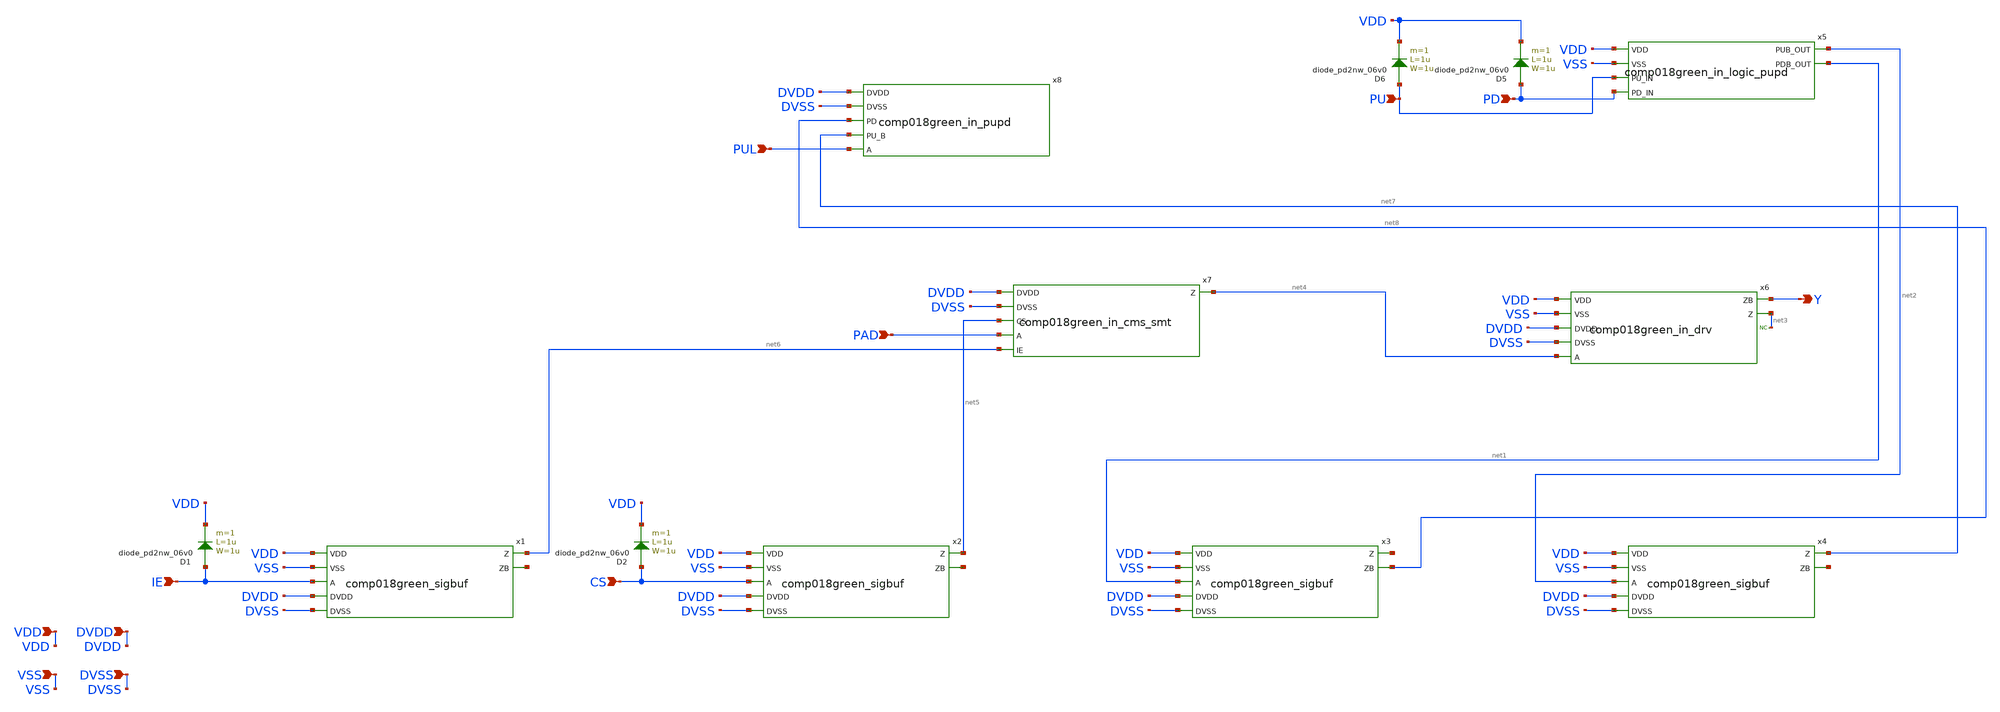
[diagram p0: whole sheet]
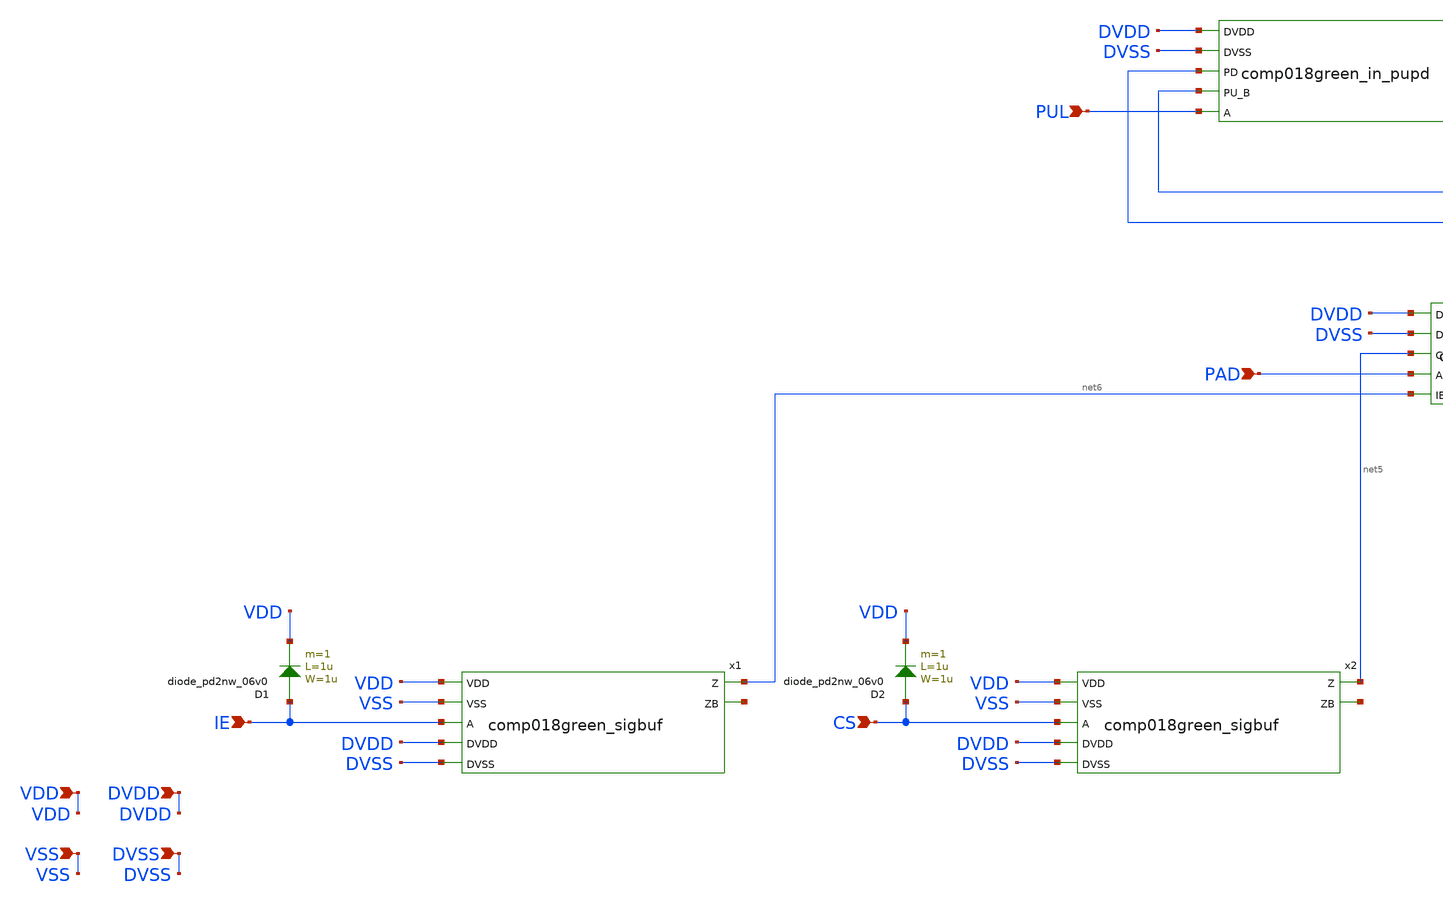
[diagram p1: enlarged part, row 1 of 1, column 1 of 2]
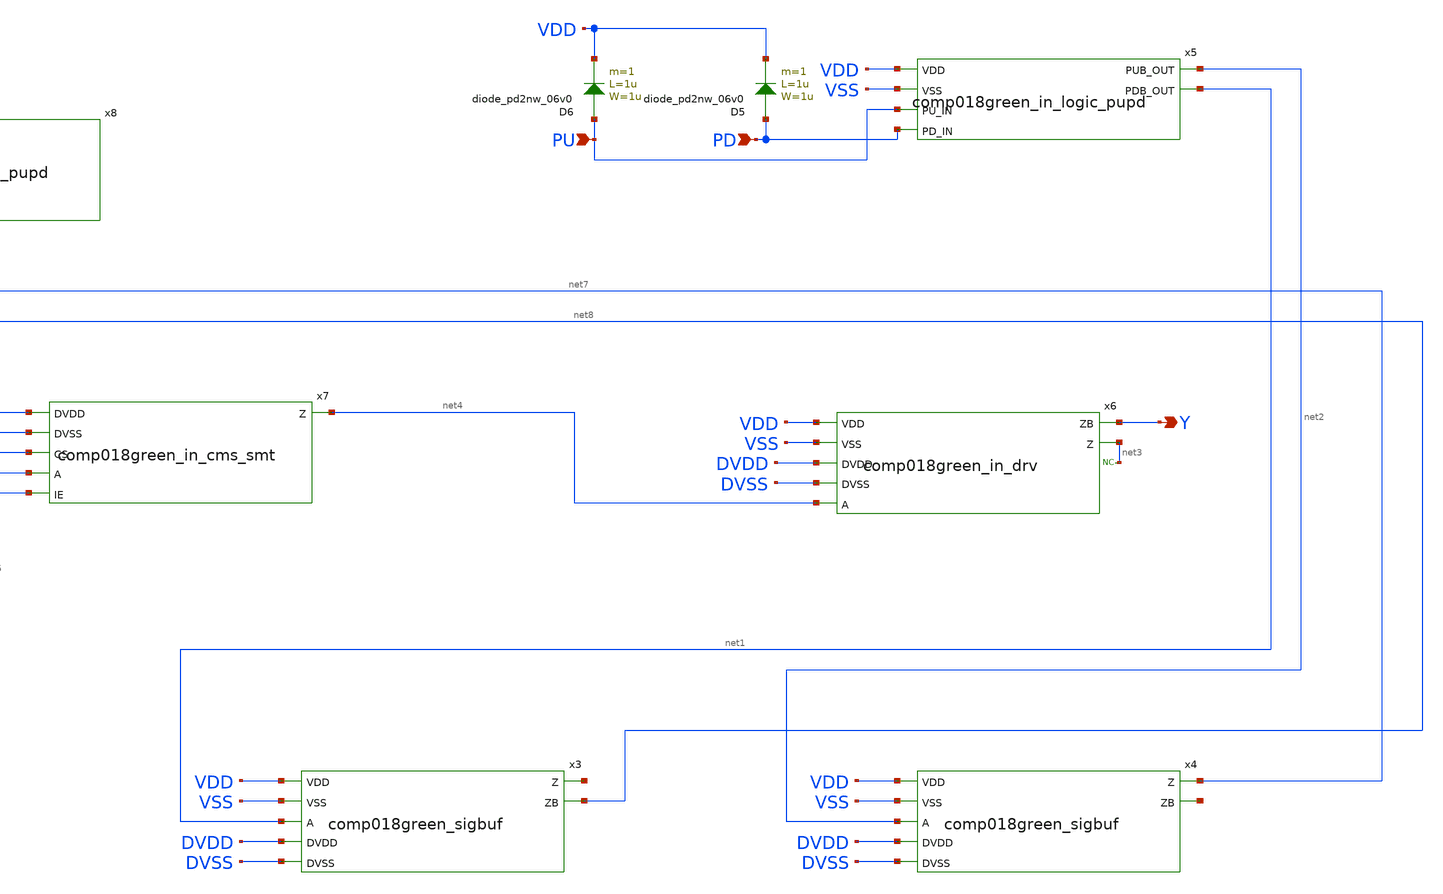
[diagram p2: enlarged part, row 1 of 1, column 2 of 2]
** sch_path: gf180mcu_fd_io__bi_24t/comp018green_inpath_cms_smt.sch
**.subckt comp018green_inpath_cms_smt IE CS VDD VSS DVDD DVSS PU PD Y PAD PUL
*.ipin IE
*.ipin CS
*.ipin VDD
*.ipin VSS
*.ipin DVDD
*.ipin DVSS
*.ipin PU
*.ipin PD
*.opin Y
*.ipin PAD
*.ipin PUL
x1 DVDD VDD net6 IE net9 DVSS VSS comp018green_sigbuf
x2 DVDD VDD net5 CS net10 DVSS VSS comp018green_sigbuf
x3 DVDD VDD net11 net1 net8 DVSS VSS comp018green_sigbuf
x4 DVDD VDD net7 net2 net12 DVSS VSS comp018green_sigbuf
D1 IE VDD diode_pd2nw_06v0 area='1u * 1u ' pj='2*1u + 2*1u ' m=1
D2 CS VDD diode_pd2nw_06v0 area='1u * 1u ' pj='2*1u + 2*1u ' m=1
x5 net2 net1 PU VDD PD VSS comp018green_in_logic_pupd
D5 PD VDD diode_pd2nw_06v0 area='1u * 1u ' pj='2*1u + 2*1u ' m=1
D6 PU VDD diode_pd2nw_06v0 area='1u * 1u ' pj='2*1u + 2*1u ' m=1
x6 Y VDD net3 net4 DVDD DVSS VSS comp018green_in_drv
* noconn #net3
x7 DVDD net4 DVSS net5 PAD net6 comp018green_in_cms_smt
x8 DVSS DVDD net8 net7 PUL comp018green_in_pupd
**.ends

* expanding   symbol:  comp018green_sigbuf.sym # of pins=7
** sym_path: gf180mcu_fd_io__bi_24t/comp018green_sigbuf.sym
** sch_path: gf180mcu_fd_io__bi_24t/comp018green_sigbuf.sch
.subckt comp018green_sigbuf DVDD VDD Z A ZB DVSS VSS
*.ipin VDD
*.ipin VSS
*.ipin A
*.ipin DVSS
*.ipin DVDD
*.opin Z
*.opin ZB
XM1 net1 A VSS VSS nfet_06v0 L=0.70u W=1.5u nf=1 ad='int((nf+1)/2) * W/nf * 0.18u' as='int((nf+2)/2) * W/nf * 0.18u'
+ pd='2*int((nf+1)/2) * (W/nf + 0.18u)' ps='2*int((nf+2)/2) * (W/nf + 0.18u)' nrd='0.18u / W' nrs='0.18u / W'
+ sa=0 sb=0 sd=0 m=1
XM2 net1 A VDD VDD pfet_06v0 L=0.70u W=3u nf=1 ad='int((nf+1)/2) * W/nf * 0.18u' as='int((nf+2)/2) * W/nf * 0.18u'
+ pd='2*int((nf+1)/2) * (W/nf + 0.18u)' ps='2*int((nf+2)/2) * (W/nf + 0.18u)' nrd='0.18u / W' nrs='0.18u / W'
+ sa=0 sb=0 sd=0 m=1
XM3 Z net1 DVDD DVDD pfet_06v0 L=0.70u W=3u nf=1 ad='int((nf+1)/2) * W/nf * 0.18u' as='int((nf+2)/2) * W/nf * 0.18u'
+ pd='2*int((nf+1)/2) * (W/nf + 0.18u)' ps='2*int((nf+2)/2) * (W/nf + 0.18u)' nrd='0.18u / W' nrs='0.18u / W'
+ sa=0 sb=0 sd=0 m=1
XM4 Z net1 DVSS DVSS nfet_06v0 L=0.70u W=1.5u nf=1 ad='int((nf+1)/2) * W/nf * 0.18u' as='int((nf+2)/2) * W/nf * 0.18u'
+ pd='2*int((nf+1)/2) * (W/nf + 0.18u)' ps='2*int((nf+2)/2) * (W/nf + 0.18u)' nrd='0.18u / W' nrs='0.18u / W'
+ sa=0 sb=0 sd=0 m=1
XM5 Z net1 DVDD DVDD pfet_06v0 L=0.70u W=3u nf=1 ad='int((nf+1)/2) * W/nf * 0.18u' as='int((nf+2)/2) * W/nf * 0.18u'
+ pd='2*int((nf+1)/2) * (W/nf + 0.18u)' ps='2*int((nf+2)/2) * (W/nf + 0.18u)' nrd='0.18u / W' nrs='0.18u / W'
+ sa=0 sb=0 sd=0 m=1
XM6 ZB Z DVDD DVDD pfet_06v0 L=0.70u W=3u nf=1 ad='int((nf+1)/2) * W/nf * 0.18u' as='int((nf+2)/2) * W/nf * 0.18u'
+ pd='2*int((nf+1)/2) * (W/nf + 0.18u)' ps='2*int((nf+2)/2) * (W/nf + 0.18u)' nrd='0.18u / W' nrs='0.18u / W'
+ sa=0 sb=0 sd=0 m=1
XM7 ZB Z DVDD DVDD pfet_06v0 L=0.70u W=3u nf=1 ad='int((nf+1)/2) * W/nf * 0.18u' as='int((nf+2)/2) * W/nf * 0.18u'
+ pd='2*int((nf+1)/2) * (W/nf + 0.18u)' ps='2*int((nf+2)/2) * (W/nf + 0.18u)' nrd='0.18u / W' nrs='0.18u / W'
+ sa=0 sb=0 sd=0 m=1
XM8 Z net1 DVSS DVSS nfet_06v0 L=0.70u W=1.5u nf=1 ad='int((nf+1)/2) * W/nf * 0.18u' as='int((nf+2)/2) * W/nf * 0.18u'
+ pd='2*int((nf+1)/2) * (W/nf + 0.18u)' ps='2*int((nf+2)/2) * (W/nf + 0.18u)' nrd='0.18u / W' nrs='0.18u / W'
+ sa=0 sb=0 sd=0 m=1
XM9 ZB Z DVSS DVSS nfet_06v0 L=0.70u W=1.5u nf=1 ad='int((nf+1)/2) * W/nf * 0.18u' as='int((nf+2)/2) * W/nf * 0.18u'
+ pd='2*int((nf+1)/2) * (W/nf + 0.18u)' ps='2*int((nf+2)/2) * (W/nf + 0.18u)' nrd='0.18u / W' nrs='0.18u / W'
+ sa=0 sb=0 sd=0 m=1
XM10 ZB Z DVSS DVSS nfet_06v0 L=0.70u W=1.5u nf=1 ad='int((nf+1)/2) * W/nf * 0.18u' as='int((nf+2)/2) * W/nf * 0.18u'
+ pd='2*int((nf+1)/2) * (W/nf + 0.18u)' ps='2*int((nf+2)/2) * (W/nf + 0.18u)' nrd='0.18u / W' nrs='0.18u / W'
+ sa=0 sb=0 sd=0 m=1
.ends


* expanding   symbol:  comp018green_in_logic_pupd.sym # of pins=6
** sym_path: gf180mcu_fd_io__bi_24t/comp018green_in_logic_pupd.sym
** sch_path: gf180mcu_fd_io__bi_24t/comp018green_in_logic_pupd.sch
.subckt comp018green_in_logic_pupd PUB_OUT PDB_OUT PU_IN VDD PD_IN VSS
*.ipin VDD
*.ipin VSS
*.ipin PD_IN
*.ipin PU_IN
*.opin PUB_OUT
*.opin PDB_OUT
XM1 net1 PU_IN VSS net6 nfet_06v0 L=0.70u W=1.5u nf=1 ad='int((nf+1)/2) * W/nf * 0.18u' as='int((nf+2)/2) * W/nf * 0.18u'
+ pd='2*int((nf+1)/2) * (W/nf + 0.18u)' ps='2*int((nf+2)/2) * (W/nf + 0.18u)' nrd='0.18u / W' nrs='0.18u / W'
+ sa=0 sb=0 sd=0 m=1
XM2 PU_IN net3 net2 net7 nfet_06v0 L=0.70u W=1.5u nf=1 ad='int((nf+1)/2) * W/nf * 0.18u' as='int((nf+2)/2) * W/nf * 0.18u'
+ pd='2*int((nf+1)/2) * (W/nf + 0.18u)' ps='2*int((nf+2)/2) * (W/nf + 0.18u)' nrd='0.18u / W' nrs='0.18u / W'
+ sa=0 sb=0 sd=0 m=1
XM3 net1 PD_IN net2 net8 nfet_06v0 L=0.70u W=1.5u nf=1 ad='int((nf+1)/2) * W/nf * 0.18u' as='int((nf+2)/2) * W/nf * 0.18u'
+ pd='2*int((nf+1)/2) * (W/nf + 0.18u)' ps='2*int((nf+2)/2) * (W/nf + 0.18u)' nrd='0.18u / W' nrs='0.18u / W'
+ sa=0 sb=0 sd=0 m=1
XM4 net3 PD_IN VSS net9 nfet_06v0 L=0.70u W=1.5u nf=1 ad='int((nf+1)/2) * W/nf * 0.18u' as='int((nf+2)/2) * W/nf * 0.18u'
+ pd='2*int((nf+1)/2) * (W/nf + 0.18u)' ps='2*int((nf+2)/2) * (W/nf + 0.18u)' nrd='0.18u / W' nrs='0.18u / W'
+ sa=0 sb=0 sd=0 m=1
XM5 net1 PU_IN VDD net10 pfet_06v0 L=0.70u W=3u nf=1 ad='int((nf+1)/2) * W/nf * 0.18u' as='int((nf+2)/2) * W/nf * 0.18u'
+ pd='2*int((nf+1)/2) * (W/nf + 0.18u)' ps='2*int((nf+2)/2) * (W/nf + 0.18u)' nrd='0.18u / W' nrs='0.18u / W'
+ sa=0 sb=0 sd=0 m=1
XM6 PU_IN PD_IN net2 net11 pfet_06v0 L=0.70u W=3u nf=1 ad='int((nf+1)/2) * W/nf * 0.18u' as='int((nf+2)/2) * W/nf * 0.18u'
+ pd='2*int((nf+1)/2) * (W/nf + 0.18u)' ps='2*int((nf+2)/2) * (W/nf + 0.18u)' nrd='0.18u / W' nrs='0.18u / W'
+ sa=0 sb=0 sd=0 m=1
XM7 net12 net3 net2 net13 pfet_06v0 L=0.70u W=3u nf=1 ad='int((nf+1)/2) * W/nf * 0.18u' as='int((nf+2)/2) * W/nf * 0.18u'
+ pd='2*int((nf+1)/2) * (W/nf + 0.18u)' ps='2*int((nf+2)/2) * (W/nf + 0.18u)' nrd='0.18u / W' nrs='0.18u / W'
+ sa=0 sb=0 sd=0 m=1
XM8 net3 PD_IN VDD net14 pfet_06v0 L=0.70u W=3u nf=1 ad='int((nf+1)/2) * W/nf * 0.18u' as='int((nf+2)/2) * W/nf * 0.18u'
+ pd='2*int((nf+1)/2) * (W/nf + 0.18u)' ps='2*int((nf+2)/2) * (W/nf + 0.18u)' nrd='0.18u / W' nrs='0.18u / W'
+ sa=0 sb=0 sd=0 m=1
XM9 PUB_OUT PU_IN VDD net15 pfet_06v0 L=0.70u W=3u nf=1 ad='int((nf+1)/2) * W/nf * 0.18u' as='int((nf+2)/2) * W/nf * 0.18u'
+ pd='2*int((nf+1)/2) * (W/nf + 0.18u)' ps='2*int((nf+2)/2) * (W/nf + 0.18u)' nrd='0.18u / W' nrs='0.18u / W'
+ sa=0 sb=0 sd=0 m=1
XM10 PUB_OUT net2 VDD net16 pfet_06v0 L=0.70u W=3u nf=1 ad='int((nf+1)/2) * W/nf * 0.18u' as='int((nf+2)/2) * W/nf * 0.18u'
+ pd='2*int((nf+1)/2) * (W/nf + 0.18u)' ps='2*int((nf+2)/2) * (W/nf + 0.18u)' nrd='0.18u / W' nrs='0.18u / W'
+ sa=0 sb=0 sd=0 m=1
XM11 PDB_OUT net2 VDD net17 pfet_06v0 L=0.70u W=3u nf=1 ad='int((nf+1)/2) * W/nf * 0.18u' as='int((nf+2)/2) * W/nf * 0.18u'
+ pd='2*int((nf+1)/2) * (W/nf + 0.18u)' ps='2*int((nf+2)/2) * (W/nf + 0.18u)' nrd='0.18u / W' nrs='0.18u / W'
+ sa=0 sb=0 sd=0 m=1
XM12 PDB_OUT PD_IN VDD net18 pfet_06v0 L=0.70u W=3u nf=1 ad='int((nf+1)/2) * W/nf * 0.18u' as='int((nf+2)/2) * W/nf * 0.18u'
+ pd='2*int((nf+1)/2) * (W/nf + 0.18u)' ps='2*int((nf+2)/2) * (W/nf + 0.18u)' nrd='0.18u / W' nrs='0.18u / W'
+ sa=0 sb=0 sd=0 m=1
XM13 net4 PU_IN VSS net19 nfet_06v0 L=0.70u W=3u nf=1 ad='int((nf+1)/2) * W/nf * 0.18u' as='int((nf+2)/2) * W/nf * 0.18u'
+ pd='2*int((nf+1)/2) * (W/nf + 0.18u)' ps='2*int((nf+2)/2) * (W/nf + 0.18u)' nrd='0.18u / W' nrs='0.18u / W'
+ sa=0 sb=0 sd=0 m=1
XM14 net4 net2 PUB_OUT net20 nfet_06v0 L=0.70u W=3u nf=1 ad='int((nf+1)/2) * W/nf * 0.18u' as='int((nf+2)/2) * W/nf * 0.18u'
+ pd='2*int((nf+1)/2) * (W/nf + 0.18u)' ps='2*int((nf+2)/2) * (W/nf + 0.18u)' nrd='0.18u / W' nrs='0.18u / W'
+ sa=0 sb=0 sd=0 m=1
XM15 net5 net2 VSS net21 nfet_06v0 L=0.70u W=3u nf=1 ad='int((nf+1)/2) * W/nf * 0.18u' as='int((nf+2)/2) * W/nf * 0.18u'
+ pd='2*int((nf+1)/2) * (W/nf + 0.18u)' ps='2*int((nf+2)/2) * (W/nf + 0.18u)' nrd='0.18u / W' nrs='0.18u / W'
+ sa=0 sb=0 sd=0 m=1
XM16 net5 PD_IN PDB_OUT net22 nfet_06v0 L=0.70u W=3u nf=1 ad='int((nf+1)/2) * W/nf * 0.18u' as='int((nf+2)/2) * W/nf * 0.18u'
+ pd='2*int((nf+1)/2) * (W/nf + 0.18u)' ps='2*int((nf+2)/2) * (W/nf + 0.18u)' nrd='0.18u / W' nrs='0.18u / W'
+ sa=0 sb=0 sd=0 m=1
.ends


* expanding   symbol:  comp018green_in_drv.sym # of pins=7
** sym_path: gf180mcu_fd_io__bi_24t/comp018green_in_drv.sym
** sch_path: gf180mcu_fd_io__bi_24t/comp018green_in_drv.sch
.subckt comp018green_in_drv ZB VDD Z A DVDD DVSS VSS
*.ipin A
*.ipin DVDD
*.ipin DVSS
*.opin Z
*.opin ZB
*.ipin VDD
*.ipin VSS
XM1 DVSS A net1 net2 nfet_06v0 L=0.70u W=4u nf=1 ad='int((nf+1)/2) * W/nf * 0.18u' as='int((nf+2)/2) * W/nf * 0.18u'
+ pd='2*int((nf+1)/2) * (W/nf + 0.18u)' ps='2*int((nf+2)/2) * (W/nf + 0.18u)' nrd='0.18u / W' nrs='0.18u / W'
+ sa=0 sb=0 sd=0 m=1
XM3 net1 A DVDD net3 pfet_06v0 L=0.70u W=2u nf=1 ad='int((nf+1)/2) * W/nf * 0.18u' as='int((nf+2)/2) * W/nf * 0.18u'
+ pd='2*int((nf+1)/2) * (W/nf + 0.18u)' ps='2*int((nf+2)/2) * (W/nf + 0.18u)' nrd='0.18u / W' nrs='0.18u / W'
+ sa=0 sb=0 sd=0 m=1
XM2 DVSS A net1 net4 nfet_06v0 L=0.70u W=4u nf=1 ad='int((nf+1)/2) * W/nf * 0.18u' as='int((nf+2)/2) * W/nf * 0.18u'
+ pd='2*int((nf+1)/2) * (W/nf + 0.18u)' ps='2*int((nf+2)/2) * (W/nf + 0.18u)' nrd='0.18u / W' nrs='0.18u / W'
+ sa=0 sb=0 sd=0 m=1
XM4 Z net1 VDD net5 pfet_06v0 L=0.70u W=2.5u nf=1 ad='int((nf+1)/2) * W/nf * 0.18u' as='int((nf+2)/2) * W/nf * 0.18u'
+ pd='2*int((nf+1)/2) * (W/nf + 0.18u)' ps='2*int((nf+2)/2) * (W/nf + 0.18u)' nrd='0.18u / W' nrs='0.18u / W'
+ sa=0 sb=0 sd=0 m=1
XM5 Z net1 VDD net6 pfet_06v0 L=0.70u W=2.5u nf=1 ad='int((nf+1)/2) * W/nf * 0.18u' as='int((nf+2)/2) * W/nf * 0.18u'
+ pd='2*int((nf+1)/2) * (W/nf + 0.18u)' ps='2*int((nf+2)/2) * (W/nf + 0.18u)' nrd='0.18u / W' nrs='0.18u / W'
+ sa=0 sb=0 sd=0 m=1
XM6 Z net1 VDD net7 pfet_06v0 L=0.70u W=2.5u nf=1 ad='int((nf+1)/2) * W/nf * 0.18u' as='int((nf+2)/2) * W/nf * 0.18u'
+ pd='2*int((nf+1)/2) * (W/nf + 0.18u)' ps='2*int((nf+2)/2) * (W/nf + 0.18u)' nrd='0.18u / W' nrs='0.18u / W'
+ sa=0 sb=0 sd=0 m=1
XM7 Z net1 VDD net8 pfet_06v0 L=0.70u W=2.5u nf=1 ad='int((nf+1)/2) * W/nf * 0.18u' as='int((nf+2)/2) * W/nf * 0.18u'
+ pd='2*int((nf+1)/2) * (W/nf + 0.18u)' ps='2*int((nf+2)/2) * (W/nf + 0.18u)' nrd='0.18u / W' nrs='0.18u / W'
+ sa=0 sb=0 sd=0 m=1
XM8 Z net1 VSS net9 nfet_06v0 L=0.70u W=1.25u nf=1 ad='int((nf+1)/2) * W/nf * 0.18u' as='int((nf+2)/2) * W/nf * 0.18u'
+ pd='2*int((nf+1)/2) * (W/nf + 0.18u)' ps='2*int((nf+2)/2) * (W/nf + 0.18u)' nrd='0.18u / W' nrs='0.18u / W'
+ sa=0 sb=0 sd=0 m=1
XM9 Z net1 VSS net10 nfet_06v0 L=0.70u W=1.25u nf=1 ad='int((nf+1)/2) * W/nf * 0.18u' as='int((nf+2)/2) * W/nf * 0.18u'
+ pd='2*int((nf+1)/2) * (W/nf + 0.18u)' ps='2*int((nf+2)/2) * (W/nf + 0.18u)' nrd='0.18u / W' nrs='0.18u / W'
+ sa=0 sb=0 sd=0 m=1
XM10 ZB Z VDD net11 pfet_06v0 L=0.70u W=3.5u nf=1 ad='int((nf+1)/2) * W/nf * 0.18u' as='int((nf+2)/2) * W/nf * 0.18u'
+ pd='2*int((nf+1)/2) * (W/nf + 0.18u)' ps='2*int((nf+2)/2) * (W/nf + 0.18u)' nrd='0.18u / W' nrs='0.18u / W'
+ sa=0 sb=0 sd=0 m=1
XM11 ZB Z VSS net12 nfet_06v0 L=0.70u W=1.5u nf=1 ad='int((nf+1)/2) * W/nf * 0.18u' as='int((nf+2)/2) * W/nf * 0.18u'
+ pd='2*int((nf+1)/2) * (W/nf + 0.18u)' ps='2*int((nf+2)/2) * (W/nf + 0.18u)' nrd='0.18u / W' nrs='0.18u / W'
+ sa=0 sb=0 sd=0 m=1
XM12 ZB Z VDD net13 pfet_06v0 L=0.70u W=3.5u nf=1 ad='int((nf+1)/2) * W/nf * 0.18u' as='int((nf+2)/2) * W/nf * 0.18u'
+ pd='2*int((nf+1)/2) * (W/nf + 0.18u)' ps='2*int((nf+2)/2) * (W/nf + 0.18u)' nrd='0.18u / W' nrs='0.18u / W'
+ sa=0 sb=0 sd=0 m=1
XM13 ZB Z VDD net14 pfet_06v0 L=0.70u W=3.5u nf=1 ad='int((nf+1)/2) * W/nf * 0.18u' as='int((nf+2)/2) * W/nf * 0.18u'
+ pd='2*int((nf+1)/2) * (W/nf + 0.18u)' ps='2*int((nf+2)/2) * (W/nf + 0.18u)' nrd='0.18u / W' nrs='0.18u / W'
+ sa=0 sb=0 sd=0 m=1
XM14 ZB Z VDD net15 pfet_06v0 L=0.70u W=3.5u nf=1 ad='int((nf+1)/2) * W/nf * 0.18u' as='int((nf+2)/2) * W/nf * 0.18u'
+ pd='2*int((nf+1)/2) * (W/nf + 0.18u)' ps='2*int((nf+2)/2) * (W/nf + 0.18u)' nrd='0.18u / W' nrs='0.18u / W'
+ sa=0 sb=0 sd=0 m=1
XM15 ZB Z VDD net16 pfet_06v0 L=0.70u W=3.5u nf=1 ad='int((nf+1)/2) * W/nf * 0.18u' as='int((nf+2)/2) * W/nf * 0.18u'
+ pd='2*int((nf+1)/2) * (W/nf + 0.18u)' ps='2*int((nf+2)/2) * (W/nf + 0.18u)' nrd='0.18u / W' nrs='0.18u / W'
+ sa=0 sb=0 sd=0 m=1
XM16 ZB Z VDD net17 pfet_06v0 L=0.70u W=3.5u nf=1 ad='int((nf+1)/2) * W/nf * 0.18u' as='int((nf+2)/2) * W/nf * 0.18u'
+ pd='2*int((nf+1)/2) * (W/nf + 0.18u)' ps='2*int((nf+2)/2) * (W/nf + 0.18u)' nrd='0.18u / W' nrs='0.18u / W'
+ sa=0 sb=0 sd=0 m=1
XM17 ZB Z VSS net18 nfet_06v0 L=0.70u W=1.5u nf=1 ad='int((nf+1)/2) * W/nf * 0.18u' as='int((nf+2)/2) * W/nf * 0.18u'
+ pd='2*int((nf+1)/2) * (W/nf + 0.18u)' ps='2*int((nf+2)/2) * (W/nf + 0.18u)' nrd='0.18u / W' nrs='0.18u / W'
+ sa=0 sb=0 sd=0 m=1
XM18 ZB Z VSS net19 nfet_06v0 L=0.70u W=1.5u nf=1 ad='int((nf+1)/2) * W/nf * 0.18u' as='int((nf+2)/2) * W/nf * 0.18u'
+ pd='2*int((nf+1)/2) * (W/nf + 0.18u)' ps='2*int((nf+2)/2) * (W/nf + 0.18u)' nrd='0.18u / W' nrs='0.18u / W'
+ sa=0 sb=0 sd=0 m=1
XM19 ZB Z VSS net20 nfet_06v0 L=0.70u W=1.5u nf=1 ad='int((nf+1)/2) * W/nf * 0.18u' as='int((nf+2)/2) * W/nf * 0.18u'
+ pd='2*int((nf+1)/2) * (W/nf + 0.18u)' ps='2*int((nf+2)/2) * (W/nf + 0.18u)' nrd='0.18u / W' nrs='0.18u / W'
+ sa=0 sb=0 sd=0 m=1
XM20 ZB Z VSS net21 nfet_06v0 L=0.70u W=1.5u nf=1 ad='int((nf+1)/2) * W/nf * 0.18u' as='int((nf+2)/2) * W/nf * 0.18u'
+ pd='2*int((nf+1)/2) * (W/nf + 0.18u)' ps='2*int((nf+2)/2) * (W/nf + 0.18u)' nrd='0.18u / W' nrs='0.18u / W'
+ sa=0 sb=0 sd=0 m=1
XM21 ZB Z VSS net22 nfet_06v0 L=0.70u W=1.5u nf=1 ad='int((nf+1)/2) * W/nf * 0.18u' as='int((nf+2)/2) * W/nf * 0.18u'
+ pd='2*int((nf+1)/2) * (W/nf + 0.18u)' ps='2*int((nf+2)/2) * (W/nf + 0.18u)' nrd='0.18u / W' nrs='0.18u / W'
+ sa=0 sb=0 sd=0 m=1
.ends


* expanding   symbol:  comp018green_in_cms_smt.sym # of pins=6
** sym_path: gf180mcu_fd_io__bi_24t/comp018green_in_cms_smt.sym
** sch_path: gf180mcu_fd_io__bi_24t/comp018green_in_cms_smt.sch
.subckt comp018green_in_cms_smt DVDD Z DVSS CS A IE
*.ipin CS
*.ipin IE
*.opin Z
*.ipin A
*.ipin DVDD
*.ipin DVSS
XM1 net1 CS DVSS net7 nfet_06v0 L=0.70u W=2u nf=1 ad='int((nf+1)/2) * W/nf * 0.18u' as='int((nf+2)/2) * W/nf * 0.18u'
+ pd='2*int((nf+1)/2) * (W/nf + 0.18u)' ps='2*int((nf+2)/2) * (W/nf + 0.18u)' nrd='0.18u / W' nrs='0.18u / W'
+ sa=0 sb=0 sd=0 m=1
XM2 net1 CS DVSS net8 nfet_06v0 L=0.70u W=2u nf=1 ad='int((nf+1)/2) * W/nf * 0.18u' as='int((nf+2)/2) * W/nf * 0.18u'
+ pd='2*int((nf+1)/2) * (W/nf + 0.18u)' ps='2*int((nf+2)/2) * (W/nf + 0.18u)' nrd='0.18u / W' nrs='0.18u / W'
+ sa=0 sb=0 sd=0 m=1
XM3 net1 CS DVDD net9 pfet_06v0 L=0.70u W=4u nf=1 ad='int((nf+1)/2) * W/nf * 0.18u' as='int((nf+2)/2) * W/nf * 0.18u'
+ pd='2*int((nf+1)/2) * (W/nf + 0.18u)' ps='2*int((nf+2)/2) * (W/nf + 0.18u)' nrd='0.18u / W' nrs='0.18u / W'
+ sa=0 sb=0 sd=0 m=1
XM4 net1 CS DVDD net10 pfet_06v0 L=0.70u W=4u nf=1 ad='int((nf+1)/2) * W/nf * 0.18u' as='int((nf+2)/2) * W/nf * 0.18u'
+ pd='2*int((nf+1)/2) * (W/nf + 0.18u)' ps='2*int((nf+2)/2) * (W/nf + 0.18u)' nrd='0.18u / W' nrs='0.18u / W'
+ sa=0 sb=0 sd=0 m=1
XM5 net6 net1 DVSS net11 nfet_06v0 L=0.70u W=1.5u nf=1 ad='int((nf+1)/2) * W/nf * 0.18u' as='int((nf+2)/2) * W/nf * 0.18u'
+ pd='2*int((nf+1)/2) * (W/nf + 0.18u)' ps='2*int((nf+2)/2) * (W/nf + 0.18u)' nrd='0.18u / W' nrs='0.18u / W'
+ sa=0 sb=0 sd=0 m=1
XM6 net2 IE DVSS net12 nfet_06v0 L=0.70u W=3.2u nf=1 ad='int((nf+1)/2) * W/nf * 0.18u' as='int((nf+2)/2) * W/nf * 0.18u'
+ pd='2*int((nf+1)/2) * (W/nf + 0.18u)' ps='2*int((nf+2)/2) * (W/nf + 0.18u)' nrd='0.18u / W' nrs='0.18u / W'
+ sa=0 sb=0 sd=0 m=1
XM7 net2 IE DVSS net13 nfet_06v0 L=0.70u W=3.2u nf=1 ad='int((nf+1)/2) * W/nf * 0.18u' as='int((nf+2)/2) * W/nf * 0.18u'
+ pd='2*int((nf+1)/2) * (W/nf + 0.18u)' ps='2*int((nf+2)/2) * (W/nf + 0.18u)' nrd='0.18u / W' nrs='0.18u / W'
+ sa=0 sb=0 sd=0 m=1
XM8 net2 IE DVSS net14 nfet_06v0 L=0.70u W=3.2u nf=1 ad='int((nf+1)/2) * W/nf * 0.18u' as='int((nf+2)/2) * W/nf * 0.18u'
+ pd='2*int((nf+1)/2) * (W/nf + 0.18u)' ps='2*int((nf+2)/2) * (W/nf + 0.18u)' nrd='0.18u / W' nrs='0.18u / W'
+ sa=0 sb=0 sd=0 m=1
XM9 net2 IE DVSS net15 nfet_06v0 L=0.70u W=3.2u nf=1 ad='int((nf+1)/2) * W/nf * 0.18u' as='int((nf+2)/2) * W/nf * 0.18u'
+ pd='2*int((nf+1)/2) * (W/nf + 0.18u)' ps='2*int((nf+2)/2) * (W/nf + 0.18u)' nrd='0.18u / W' nrs='0.18u / W'
+ sa=0 sb=0 sd=0 m=1
XM10 net2 IE DVSS net16 nfet_06v0 L=0.70u W=3.2u nf=1 ad='int((nf+1)/2) * W/nf * 0.18u' as='int((nf+2)/2) * W/nf * 0.18u'
+ pd='2*int((nf+1)/2) * (W/nf + 0.18u)' ps='2*int((nf+2)/2) * (W/nf + 0.18u)' nrd='0.18u / W' nrs='0.18u / W'
+ sa=0 sb=0 sd=0 m=1
XM11 net3 CS DVDD net17 pfet_06v0 L=0.70u W=1.5u nf=1 ad='int((nf+1)/2) * W/nf * 0.18u' as='int((nf+2)/2) * W/nf * 0.18u'
+ pd='2*int((nf+1)/2) * (W/nf + 0.18u)' ps='2*int((nf+2)/2) * (W/nf + 0.18u)' nrd='0.18u / W' nrs='0.18u / W'
+ sa=0 sb=0 sd=0 m=1
XM12 net3 CS DVDD net18 pfet_06v0 L=0.70u W=1.5u nf=1 ad='int((nf+1)/2) * W/nf * 0.18u' as='int((nf+2)/2) * W/nf * 0.18u'
+ pd='2*int((nf+1)/2) * (W/nf + 0.18u)' ps='2*int((nf+2)/2) * (W/nf + 0.18u)' nrd='0.18u / W' nrs='0.18u / W'
+ sa=0 sb=0 sd=0 m=1
XM13 DVDD IE Z net19 pfet_06v0 L=0.70u W=2u nf=1 ad='int((nf+1)/2) * W/nf * 0.18u' as='int((nf+2)/2) * W/nf * 0.18u'
+ pd='2*int((nf+1)/2) * (W/nf + 0.18u)' ps='2*int((nf+2)/2) * (W/nf + 0.18u)' nrd='0.18u / W' nrs='0.18u / W'
+ sa=0 sb=0 sd=0 m=1
XM14 DVDD IE Z net20 pfet_06v0 L=0.70u W=2u nf=1 ad='int((nf+1)/2) * W/nf * 0.18u' as='int((nf+2)/2) * W/nf * 0.18u'
+ pd='2*int((nf+1)/2) * (W/nf + 0.18u)' ps='2*int((nf+2)/2) * (W/nf + 0.18u)' nrd='0.18u / W' nrs='0.18u / W'
+ sa=0 sb=0 sd=0 m=1
XM15 DVDD IE Z net21 pfet_06v0 L=0.70u W=2u nf=1 ad='int((nf+1)/2) * W/nf * 0.18u' as='int((nf+2)/2) * W/nf * 0.18u'
+ pd='2*int((nf+1)/2) * (W/nf + 0.18u)' ps='2*int((nf+2)/2) * (W/nf + 0.18u)' nrd='0.18u / W' nrs='0.18u / W'
+ sa=0 sb=0 sd=0 m=1
XM16 net2 A net4 net22 nfet_06v0 L=0.70u W=2.65u nf=1 ad='int((nf+1)/2) * W/nf * 0.18u' as='int((nf+2)/2) * W/nf * 0.18u'
+ pd='2*int((nf+1)/2) * (W/nf + 0.18u)' ps='2*int((nf+2)/2) * (W/nf + 0.18u)' nrd='0.18u / W' nrs='0.18u / W'
+ sa=0 sb=0 sd=0 m=1
XM17 net2 A net4 net23 nfet_06v0 L=0.70u W=2.65u nf=1 ad='int((nf+1)/2) * W/nf * 0.18u' as='int((nf+2)/2) * W/nf * 0.18u'
+ pd='2*int((nf+1)/2) * (W/nf + 0.18u)' ps='2*int((nf+2)/2) * (W/nf + 0.18u)' nrd='0.18u / W' nrs='0.18u / W'
+ sa=0 sb=0 sd=0 m=1
XM18 net2 A net4 net24 nfet_06v0 L=0.70u W=2.65u nf=1 ad='int((nf+1)/2) * W/nf * 0.18u' as='int((nf+2)/2) * W/nf * 0.18u'
+ pd='2*int((nf+1)/2) * (W/nf + 0.18u)' ps='2*int((nf+2)/2) * (W/nf + 0.18u)' nrd='0.18u / W' nrs='0.18u / W'
+ sa=0 sb=0 sd=0 m=1
XM19 net2 A net4 net25 nfet_06v0 L=0.70u W=2.65u nf=1 ad='int((nf+1)/2) * W/nf * 0.18u' as='int((nf+2)/2) * W/nf * 0.18u'
+ pd='2*int((nf+1)/2) * (W/nf + 0.18u)' ps='2*int((nf+2)/2) * (W/nf + 0.18u)' nrd='0.18u / W' nrs='0.18u / W'
+ sa=0 sb=0 sd=0 m=1
XM20 net4 A Z net26 nfet_06v0 L=0.70u W=3u nf=1 ad='int((nf+1)/2) * W/nf * 0.18u' as='int((nf+2)/2) * W/nf * 0.18u'
+ pd='2*int((nf+1)/2) * (W/nf + 0.18u)' ps='2*int((nf+2)/2) * (W/nf + 0.18u)' nrd='0.18u / W' nrs='0.18u / W'
+ sa=0 sb=0 sd=0 m=1
XM21 net4 A Z net27 nfet_06v0 L=0.70u W=3u nf=1 ad='int((nf+1)/2) * W/nf * 0.18u' as='int((nf+2)/2) * W/nf * 0.18u'
+ pd='2*int((nf+1)/2) * (W/nf + 0.18u)' ps='2*int((nf+2)/2) * (W/nf + 0.18u)' nrd='0.18u / W' nrs='0.18u / W'
+ sa=0 sb=0 sd=0 m=1
XM22 net4 A Z net28 nfet_06v0 L=0.70u W=3u nf=1 ad='int((nf+1)/2) * W/nf * 0.18u' as='int((nf+2)/2) * W/nf * 0.18u'
+ pd='2*int((nf+1)/2) * (W/nf + 0.18u)' ps='2*int((nf+2)/2) * (W/nf + 0.18u)' nrd='0.18u / W' nrs='0.18u / W'
+ sa=0 sb=0 sd=0 m=1
XM23 net4 A Z net29 nfet_06v0 L=0.70u W=3u nf=1 ad='int((nf+1)/2) * W/nf * 0.18u' as='int((nf+2)/2) * W/nf * 0.18u'
+ pd='2*int((nf+1)/2) * (W/nf + 0.18u)' ps='2*int((nf+2)/2) * (W/nf + 0.18u)' nrd='0.18u / W' nrs='0.18u / W'
+ sa=0 sb=0 sd=0 m=1
XM24 DVDD A net5 net30 pfet_06v0 L=0.70u W=1.9u nf=1 ad='int((nf+1)/2) * W/nf * 0.18u' as='int((nf+2)/2) * W/nf * 0.18u'
+ pd='2*int((nf+1)/2) * (W/nf + 0.18u)' ps='2*int((nf+2)/2) * (W/nf + 0.18u)' nrd='0.18u / W' nrs='0.18u / W'
+ sa=0 sb=0 sd=0 m=1
XM25 DVDD A net5 net31 pfet_06v0 L=0.70u W=1.9u nf=1 ad='int((nf+1)/2) * W/nf * 0.18u' as='int((nf+2)/2) * W/nf * 0.18u'
+ pd='2*int((nf+1)/2) * (W/nf + 0.18u)' ps='2*int((nf+2)/2) * (W/nf + 0.18u)' nrd='0.18u / W' nrs='0.18u / W'
+ sa=0 sb=0 sd=0 m=1
XM26 Z A net5 net32 pfet_06v0 L=0.70u W=2.15u nf=1 ad='int((nf+1)/2) * W/nf * 0.18u' as='int((nf+2)/2) * W/nf * 0.18u'
+ pd='2*int((nf+1)/2) * (W/nf + 0.18u)' ps='2*int((nf+2)/2) * (W/nf + 0.18u)' nrd='0.18u / W' nrs='0.18u / W'
+ sa=0 sb=0 sd=0 m=1
XM27 Z A net5 net33 pfet_06v0 L=0.70u W=2.15u nf=1 ad='int((nf+1)/2) * W/nf * 0.18u' as='int((nf+2)/2) * W/nf * 0.18u'
+ pd='2*int((nf+1)/2) * (W/nf + 0.18u)' ps='2*int((nf+2)/2) * (W/nf + 0.18u)' nrd='0.18u / W' nrs='0.18u / W'
+ sa=0 sb=0 sd=0 m=1
XM28 DVSS net3 net5 net34 pfet_06v0 L=0.70u W=1.9u nf=1 ad='int((nf+1)/2) * W/nf * 0.18u' as='int((nf+2)/2) * W/nf * 0.18u'
+ pd='2*int((nf+1)/2) * (W/nf + 0.18u)' ps='2*int((nf+2)/2) * (W/nf + 0.18u)' nrd='0.18u / W' nrs='0.18u / W'
+ sa=0 sb=0 sd=0 m=1
XM29 DVSS net3 net5 net35 pfet_06v0 L=0.70u W=1.9u nf=1 ad='int((nf+1)/2) * W/nf * 0.18u' as='int((nf+2)/2) * W/nf * 0.18u'
+ pd='2*int((nf+1)/2) * (W/nf + 0.18u)' ps='2*int((nf+2)/2) * (W/nf + 0.18u)' nrd='0.18u / W' nrs='0.18u / W'
+ sa=0 sb=0 sd=0 m=1
XM30 DVDD net6 net4 net36 nfet_06v0 L=0.70u W=1.3u nf=1 ad='int((nf+1)/2) * W/nf * 0.18u' as='int((nf+2)/2) * W/nf * 0.18u'
+ pd='2*int((nf+1)/2) * (W/nf + 0.18u)' ps='2*int((nf+2)/2) * (W/nf + 0.18u)' nrd='0.18u / W' nrs='0.18u / W'
+ sa=0 sb=0 sd=0 m=1
XM31 Z CS net3 net37 nfet_06v0 L=0.70u W=1.5u nf=1 ad='int((nf+1)/2) * W/nf * 0.18u' as='int((nf+2)/2) * W/nf * 0.18u'
+ pd='2*int((nf+1)/2) * (W/nf + 0.18u)' ps='2*int((nf+2)/2) * (W/nf + 0.18u)' nrd='0.18u / W' nrs='0.18u / W'
+ sa=0 sb=0 sd=0 m=1
XM32 Z CS net6 net38 nfet_06v0 L=0.70u W=1.5u nf=1 ad='int((nf+1)/2) * W/nf * 0.18u' as='int((nf+2)/2) * W/nf * 0.18u'
+ pd='2*int((nf+1)/2) * (W/nf + 0.18u)' ps='2*int((nf+2)/2) * (W/nf + 0.18u)' nrd='0.18u / W' nrs='0.18u / W'
+ sa=0 sb=0 sd=0 m=1
XM33 net3 net1 Z net39 pfet_06v0 L=0.70u W=2u nf=1 ad='int((nf+1)/2) * W/nf * 0.18u' as='int((nf+2)/2) * W/nf * 0.18u'
+ pd='2*int((nf+1)/2) * (W/nf + 0.18u)' ps='2*int((nf+2)/2) * (W/nf + 0.18u)' nrd='0.18u / W' nrs='0.18u / W'
+ sa=0 sb=0 sd=0 m=1
XM34 Z net1 net6 net40 pfet_06v0 L=0.70u W=2u nf=1 ad='int((nf+1)/2) * W/nf * 0.18u' as='int((nf+2)/2) * W/nf * 0.18u'
+ pd='2*int((nf+1)/2) * (W/nf + 0.18u)' ps='2*int((nf+2)/2) * (W/nf + 0.18u)' nrd='0.18u / W' nrs='0.18u / W'
+ sa=0 sb=0 sd=0 m=1
.ends


* expanding   symbol:  comp018green_in_pupd.sym # of pins=5
** sym_path: gf180mcu_fd_io__bi_24t/comp018green_in_pupd.sym
** sch_path: gf180mcu_fd_io__bi_24t/comp018green_in_pupd.sch
.subckt comp018green_in_pupd DVSS DVDD PD PU_B A
*.ipin DVDD
*.ipin DVSS
*.ipin PD
*.ipin PU_B
*.ipin A
XM1 net1 PD DVSS DVSS nfet_06v0 L=0.70u W=1.5u nf=1 ad='int((nf+1)/2) * W/nf * 0.18u' as='int((nf+2)/2) * W/nf * 0.18u'
+ pd='2*int((nf+1)/2) * (W/nf + 0.18u)' ps='2*int((nf+2)/2) * (W/nf + 0.18u)' nrd='0.18u / W' nrs='0.18u / W'
+ sa=0 sb=0 sd=0 m=1
XM2 net1 PU_B DVDD DVDD pfet_06v0 L=0.70u W=3u nf=1 ad='int((nf+1)/2) * W/nf * 0.18u' as='int((nf+2)/2) * W/nf * 0.18u'
+ pd='2*int((nf+1)/2) * (W/nf + 0.18u)' ps='2*int((nf+2)/2) * (W/nf + 0.18u)' nrd='0.18u / W' nrs='0.18u / W'
+ sa=0 sb=0 sd=0 m=1
XR1 net1 net2 DVDD ppolyf_u r_width=8e-7 r_length=3.57e-5 m=1
XR2 net2 net3 DVDD ppolyf_u r_width=8e-7 r_length=3.57e-5 m=1
XR3 net3 net4 DVDD ppolyf_u r_width=8e-7 r_length=3.57e-5 m=1
XR4 net4 net5 DVDD ppolyf_u r_width=8e-7 r_length=3.57e-5 m=1
XR5 net5 net6 DVDD ppolyf_u r_width=8e-7 r_length=3.57e-5 m=1
XR6 net6 net7 DVDD ppolyf_u r_width=8e-7 r_length=3.57e-5 m=1
XR7 net7 net8 DVDD ppolyf_u r_width=8e-7 r_length=3.57e-5 m=1
XR8 net8 A DVDD ppolyf_u r_width=8e-7 r_length=2.3e-5 m=1
.ends

.end
